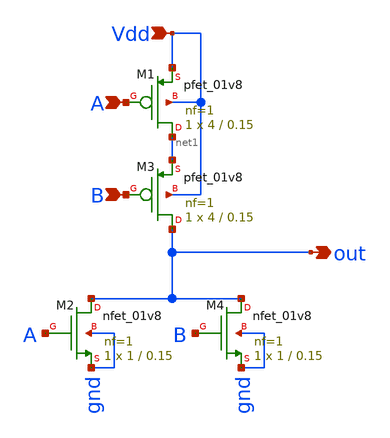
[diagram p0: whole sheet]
** sch_path: extra_stuff/nor.sch
**.subckt nor A B Vdd out
*.ipin A
*.ipin B
*.ipin Vdd
*.opin out
XM1 net1 A Vdd Vdd sky130_fd_pr__pfet_01v8 L=0.15 W=4 nf=1 ad='int((1 + 1)/2) * 4 / 1 * 0.29' as='int((1 + 2)/2) * 4 / 1 * 0.29'
+ pd='2*int((1 + 1)/2) * (4 / 1 + 0.29)' ps='2*int((1 + 2)/2) * (4 / 1 + 0.29)' nrd='0.29 / 4 ' nrs='0.29 / 4 '
+ sa=0 sb=0 sd=0 mult=1 m=1
XM2 out A gnd gnd sky130_fd_pr__nfet_01v8 L=0.15 W=1 nf=1 ad='int((1 + 1)/2) * 1 / 1 * 0.29' as='int((1 + 2)/2) * 1 / 1 * 0.29'
+ pd='2*int((1 + 1)/2) * (1 / 1 + 0.29)' ps='2*int((1 + 2)/2) * (1 / 1 + 0.29)' nrd='0.29 / 1 ' nrs='0.29 / 1 '
+ sa=0 sb=0 sd=0 mult=1 m=1
XM3 out B net1 Vdd sky130_fd_pr__pfet_01v8 L=0.15 W=4 nf=1 ad='int((1 + 1)/2) * 4 / 1 * 0.29' as='int((1 + 2)/2) * 4 / 1 * 0.29'
+ pd='2*int((1 + 1)/2) * (4 / 1 + 0.29)' ps='2*int((1 + 2)/2) * (4 / 1 + 0.29)' nrd='0.29 / 4 ' nrs='0.29 / 4 '
+ sa=0 sb=0 sd=0 mult=1 m=1
XM4 out B gnd gnd sky130_fd_pr__nfet_01v8 L=0.15 W=1 nf=1 ad='int((1 + 1)/2) * 1 / 1 * 0.29' as='int((1 + 2)/2) * 1 / 1 * 0.29'
+ pd='2*int((1 + 1)/2) * (1 / 1 + 0.29)' ps='2*int((1 + 2)/2) * (1 / 1 + 0.29)' nrd='0.29 / 1 ' nrs='0.29 / 1 '
+ sa=0 sb=0 sd=0 mult=1 m=1
**.ends
.end
